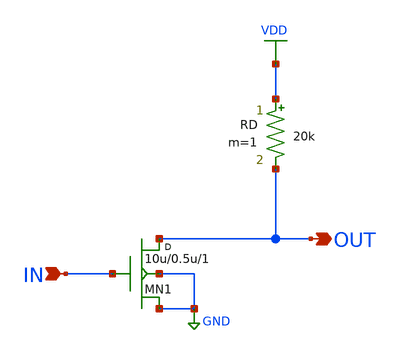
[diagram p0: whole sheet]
** sch_path: E3_238_Analog_VLSI_Circuits/12_Amplifier_Noise/cs_noise.sch
**.subckt cs_noise IN OUT
*.ipin IN
*.opin OUT
MN1 OUT IN GND GND nmos w=10u l=0.5u m=1
RD VDD OUT 20k m=1
**** begin user architecture code

.include /home/anirudh/Analog_VLSI_Projects/models/cmos_180nm.mod
VDD VDD 0 DC 1.8
VIN IN 0 DC 0.57 AC 1
CL OUT GND 1p

.control
  op
  noise v(OUT) VIN dec 10 10 100Meg
  plot onoise_spectrum
  plot inoise_spectrum
.endc


**** end user architecture code
**.ends
.GLOBAL VDD
.GLOBAL GND
.end
